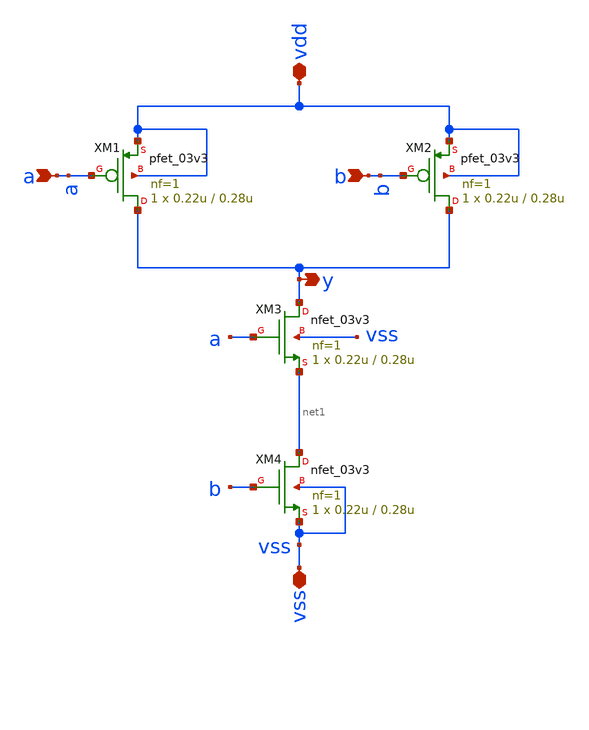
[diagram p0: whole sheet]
** sch_path: xschem/sar_adc/blocks/comparator/comp_nand_3v3.sch
**.subckt comp_nand_3v3 vdd vss y a b
*.iopin vdd
*.iopin vss
*.opin y
*.ipin a
*.ipin b
XM1 y a vdd vdd pfet_03v3 L=0.28u W=0.22u nf=1 ad='int((nf+1)/2) * W/nf * 0.18u' as='int((nf+2)/2) * W/nf * 0.18u'
+ pd='2*int((nf+1)/2) * (W/nf + 0.18u)' ps='2*int((nf+2)/2) * (W/nf + 0.18u)' nrd='0.18u / W' nrs='0.18u / W'
+ sa=0 sb=0 sd=0 m=1
XM2 y b vdd vdd pfet_03v3 L=0.28u W=0.22u nf=1 ad='int((nf+1)/2) * W/nf * 0.18u' as='int((nf+2)/2) * W/nf * 0.18u'
+ pd='2*int((nf+1)/2) * (W/nf + 0.18u)' ps='2*int((nf+2)/2) * (W/nf + 0.18u)' nrd='0.18u / W' nrs='0.18u / W'
+ sa=0 sb=0 sd=0 m=1
XM3 y a net1 vss nfet_03v3 L=0.28u W=0.22u nf=1 ad='int((nf+1)/2) * W/nf * 0.18u' as='int((nf+2)/2) * W/nf * 0.18u'
+ pd='2*int((nf+1)/2) * (W/nf + 0.18u)' ps='2*int((nf+2)/2) * (W/nf + 0.18u)' nrd='0.18u / W' nrs='0.18u / W'
+ sa=0 sb=0 sd=0 m=1
XM4 net1 b vss vss nfet_03v3 L=0.28u W=0.22u nf=1 ad='int((nf+1)/2) * W/nf * 0.18u' as='int((nf+2)/2) * W/nf * 0.18u'
+ pd='2*int((nf+1)/2) * (W/nf + 0.18u)' ps='2*int((nf+2)/2) * (W/nf + 0.18u)' nrd='0.18u / W' nrs='0.18u / W'
+ sa=0 sb=0 sd=0 m=1
**.ends
.end
